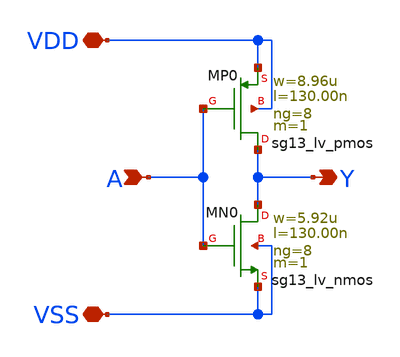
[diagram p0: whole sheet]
** sch_path: xschem/inv_8.sch
**.subckt inv_8 Y A VDD VSS
*.opin Y
*.ipin A
*.iopin VDD
*.iopin VSS
XMN0 Y A VSS VSS sg13_lv_nmos w=5.92u l=130.00n ng=8 m=1 mm_ok=1
XMP0 Y A VDD VDD sg13_lv_pmos w=8.96u l=130.00n ng=8 m=1 mm_ok=1
**.ends
.end
